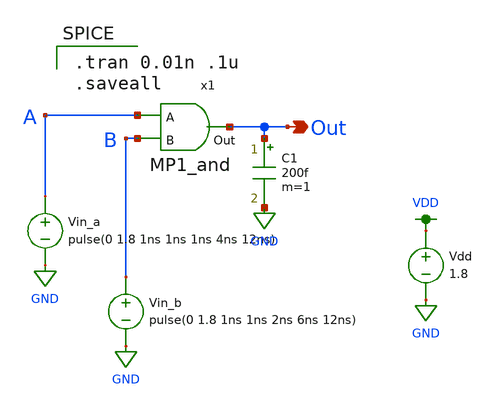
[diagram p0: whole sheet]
** sch_path: miniproject2/MP1_LAB.sch
**.subckt MP1_LAB Out
*.opin Out
x1 A Out B MP1_and
Vdd VDD GND 1.8
Vin_a A GND pulse(0 1.8 1ns 1ns 1ns 4ns 12ns)
C1 Out GND 200f m=1
Vin_b B GND pulse(0 1.8 1ns 1ns 2ns 6ns 12ns)
**** begin user architecture code

.option wnflag=1
.lib ~/skywater/skywater-pdk/libraries/sky130_fd_pr_ngspice/latest/models/sky130.lib.spice tt


.tran 0.01n .1u
.saveall

**** end user architecture code
**.ends
.GLOBAL GND
.GLOBAL VDD
.end
